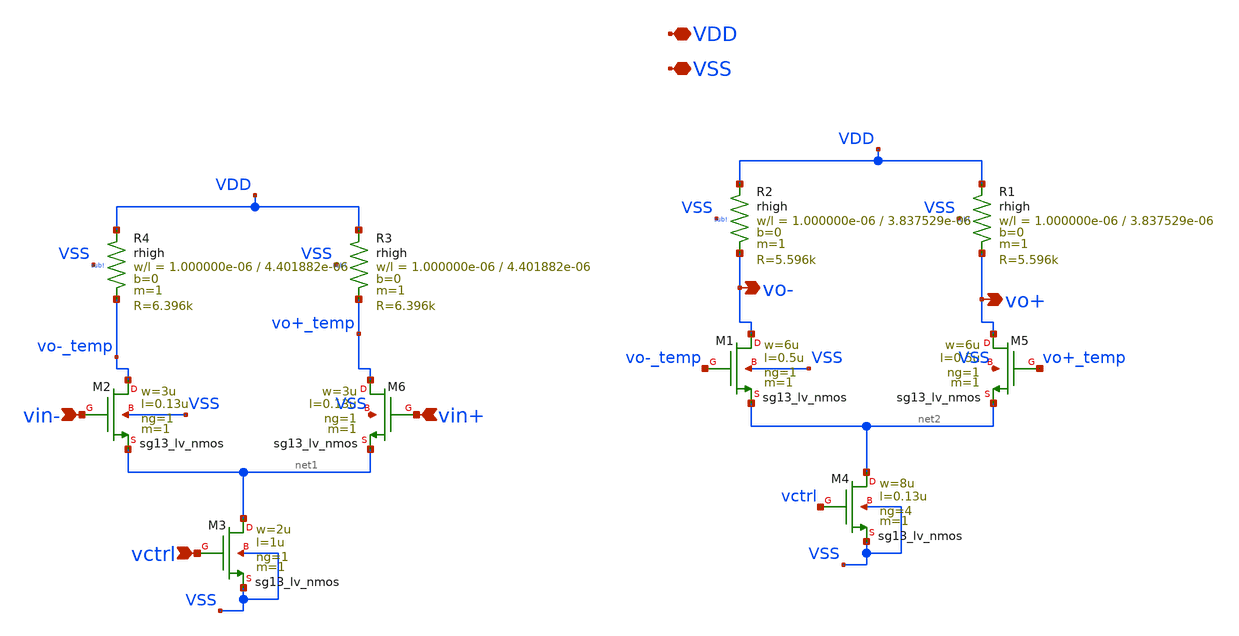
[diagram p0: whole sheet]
** sch_path: xschem/diff_amp_inv.sch
**.subckt diff_amp_inv VDD VSS vin- vctrl vin+ vo+ vo-
*.iopin VDD
*.iopin VSS
*.ipin vin-
*.ipin vctrl
*.ipin vin+
*.opin vo+
*.opin vo-
XM2 vo-_temp vin- net1 VSS sg13_lv_nmos w=3u l=0.13u ng=1 m=1 mm_ok=1
XM3 net1 vctrl VSS VSS sg13_lv_nmos w=2u l=1u ng=1 m=1 mm_ok=1
XM6 vo+_temp vin+ net1 VSS sg13_lv_nmos w=3u l=0.13u ng=1 m=1 mm_ok=1
XR3 VDD vo+_temp sub! rhigh w=1.000000e-06 l=4.401882e-06 m=1 b=0 mm_ok=1
XR4 VDD vo-_temp sub! rhigh w=1.000000e-06 l=4.401882e-06 m=1 b=0 mm_ok=1
XM1 vo- vo-_temp net2 VSS sg13_lv_nmos w=6u l=0.5u ng=1 m=1 mm_ok=1
XM4 net2 vctrl VSS VSS sg13_lv_nmos w=8u l=0.13u ng=4 m=1 mm_ok=1
XM5 vo+ vo+_temp net2 VSS sg13_lv_nmos w=6u l=0.5u ng=1 m=1 mm_ok=1
XR1 VDD vo+ sub! rhigh w=1.000000e-06 l=3.837529e-06 m=1 b=0 mm_ok=1
XR2 VDD vo- sub! rhigh w=1.000000e-06 l=3.837529e-06 m=1 b=0 mm_ok=1
**.ends
.end
